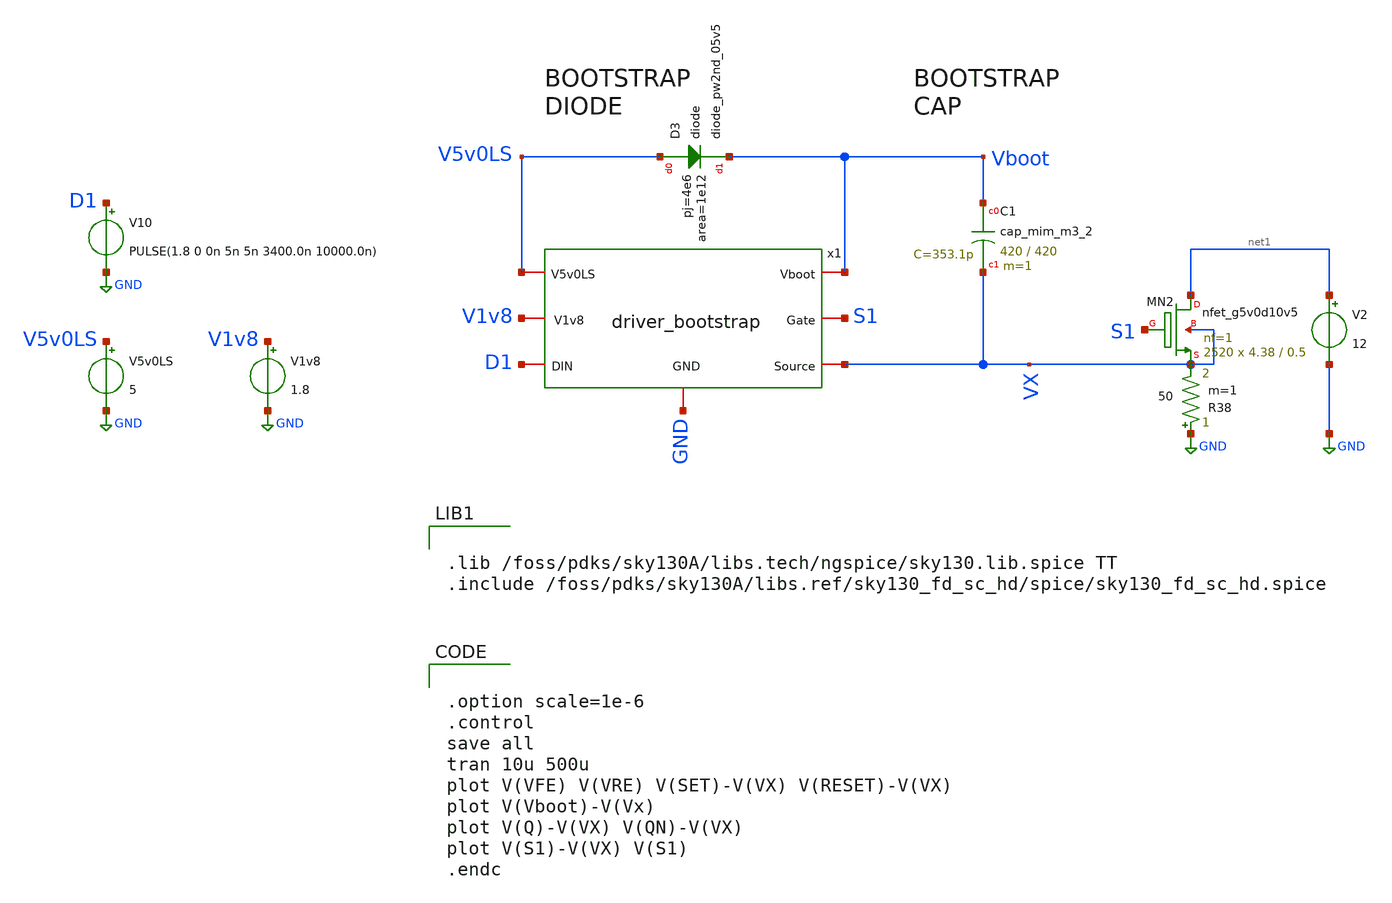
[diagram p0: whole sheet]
** sch_path: xschem/test/tb_driver_bootstrap.sch
**.subckt tb_driver_bootstrap
V5v0LS V5v0LS GND 5
XMN2 net1 S1 VX VX sky130_fd_pr__nfet_g5v0d10v5 L=0.5 W=4.38 nf=1 ad='int((nf+1)/2) * W/nf * 0.29' as='int((nf+2)/2) * W/nf * 0.29'
+ pd='2*int((nf+1)/2) * (W/nf + 0.29)' ps='2*int((nf+2)/2) * (W/nf + 0.29)' nrd='0.29 / W' nrs='0.29 / W'
+ sa=0 sb=0 sd=0 mult=2520 m=2520
V2 net1 GND 12
R38 GND VX 50 m=1
V1v8 V1v8 GND 1.8
V10 D1 GND PULSE(1.8 0 0n 5n 5n 3400.0n 10000.0n)
x1 Vboot S1 VX V5v0LS V1v8 GND D1 driver_bootstrap
XD3 V5v0LS Vboot sky130_fd_pr__diode_pw2nd_05v5 area=1e12 pj=4e6
XC1 Vboot VX sky130_fd_pr__cap_mim_m3_2 W=420 L=420 MF=1 m=1
**** begin user architecture code


.lib /foss/pdks/sky130A/libs.tech/ngspice/sky130.lib.spice TT
.include /foss/pdks/sky130A/libs.ref/sky130_fd_sc_hd/spice/sky130_fd_sc_hd.spice




.option scale=1e-6
.control
save all
tran 10u 500u
plot V(VFE) V(VRE) V(SET)-V(VX) V(RESET)-V(VX)
plot V(Vboot)-V(Vx)
plot V(Q)-V(VX) V(QN)-V(VX)
plot V(S1)-V(VX) V(S1)
.endc


**** end user architecture code
**.ends
.GLOBAL GND
.end
